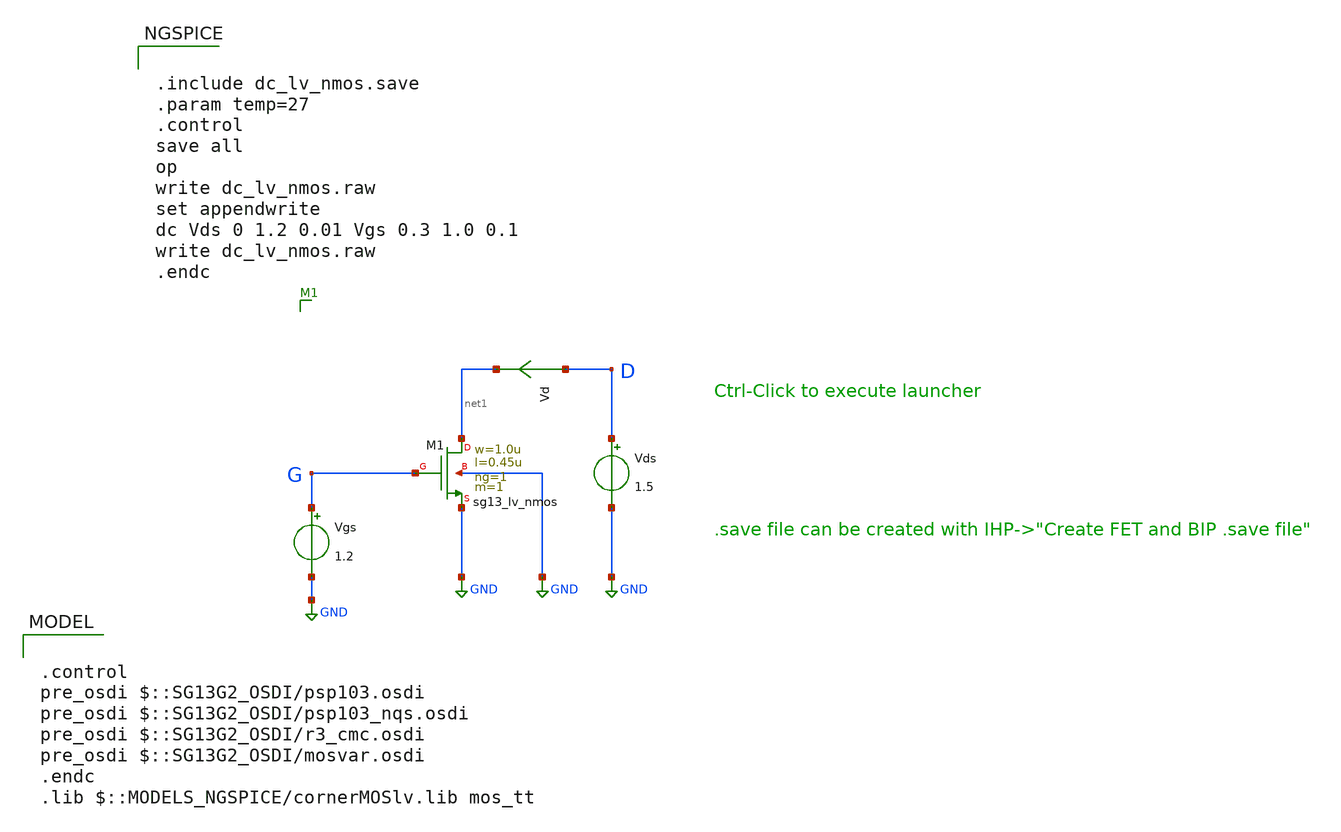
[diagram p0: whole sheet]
** sch_path: ihp-sg13g2/xschem_libs/sg13g2_tests/dc_lv_nmos/schematic/dc_lv_nmos.sch
* Copyright 2023 IHP PDK Authors
**.subckt dc_lv_nmos
Vgs G GND 1.2
Vds D GND 1.5
Vd D net1 0
.save i(vd)
XM1 net1 G GND GND sg13_lv_nmos w=1.0u l=0.45u ng=1 m=1 mm_ok=1
**** begin user architecture code

.control
pre_osdi $::SG13G2_OSDI/psp103.osdi
pre_osdi $::SG13G2_OSDI/psp103_nqs.osdi
pre_osdi $::SG13G2_OSDI/r3_cmc.osdi
pre_osdi $::SG13G2_OSDI/mosvar.osdi
.endc
.lib $::MODELS_NGSPICE/cornerMOSlv.lib mos_tt



.include dc_lv_nmos.save
.param temp=27
.control
save all
op
write dc_lv_nmos.raw
set appendwrite
dc Vds 0 1.2 0.01 Vgs 0.3 1.0 0.1
write dc_lv_nmos.raw
.endc


**** end user architecture code
**.ends
.GLOBAL GND
.end
